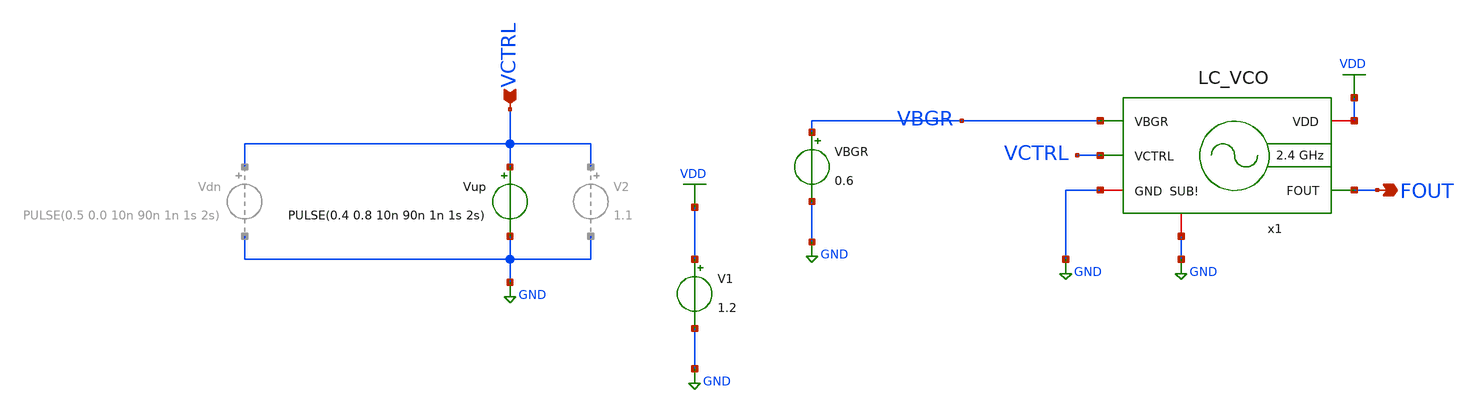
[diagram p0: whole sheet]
** sch_path: xschem/lc-vco/LC_VCO_tb.sch
**.subckt LC_VCO_tb FOUT VCTRL
*.opin FOUT
*.ipin VCTRL
VBGR VBGR GND 0.6
x1 VDD VCTRL GND FOUT VBGR GND LC_VCO
V1 VDD GND 1.2
Vup VCTRL GND PULSE(0.4 0.8 10n 90n 1n 1s 2s)
**** begin user architecture code



.param temp = 27
.options method=gear rshunt=1.0e12

.control

* Save required signals
save v(VCTRL) v(FOUT) v(x1.Vx) v(x1.OUTp)

* Long transient simulation
tran 10p 500n 100n

* Save raw waveform
write tb_LC_VCO_tran.raw

* Plot transient waveform
let vout = v(FOUT)
plot v(VCTRL) v(x1.Vx) v(FOUT) v(x1.OUTp)

* Plot steady-state waveform
plot v(VCTRL) v(x1.Vx) v(FOUT) v(x1.OUTp) xlimit 400n 405n

* FFT analysis
setplot tran1
linearize vout
set specwindow=blackman
fft vout

* Plot FFT spectrum
let power_out_db = db(vout)
plot power_out_db xlimit 2.34G 2.54G ylimit -200 0

* Find the maximum magnitude value between 2G and 3G
meas sp max_power_out_db max power_out_db FROM=2G TO=3G

* Save FFT spectrum as raw file
write LC_VCO_fft.raw frequency power_out_db
shell python3 ../xschem/lc-vco/raw_spectrum_as_tran.py LC_VCO_fft.raw

* Save FFT data
wrdata fft_output_standalone.txt frequency power_out_db

* Save waveform for external processing
wrdata vco_waveform_standalone.txt power_out_db

.endc






.param temp=27
.control
save all
op
write LC_VCO_tb.raw
.endc




.include 4nH_INDUCTOR.spice


.lib cornerMOSlv.lib mos_tt
.lib cornerMOShv.lib mos_tt
.lib cornerRES.lib res_typ
.lib cornerCAP.lib cap_typ

**** end user architecture code
**.ends

* expanding   symbol:  xschem/lc-vco/LC_VCO.sym # of pins=6
** sym_path: xschem/lc-vco/LC_VCO.sym
** sch_path: xschem/lc-vco/LC_VCO.sch
.subckt LC_VCO VDD VCTRL GND FOUT VBGR SUB!
*.opin FOUT
*.ipin VCTRL
*.ipin VBGR
*.iopin VDD
*.iopin GND
*.iopin SUB!
x1 OUTn OUTp 4nH_INDUCTOR
**** begin user architecture code


.subckt 4nH_INDUCTOR 1 2
* LVS black-box stub only
* Full model is available in 4nH_INDUCTOR.spice
.ends


**** end user architecture code
XM5 Vx Vgs GND SUB! sg13_lv_nmos w=384u l=1u ng=48 m=1 mm_ok=1
XM4 OUTp OUTn VDD NW sg13_lv_pmos w=36u l=0.13u ng=5 m=1 mm_ok=1
XM3 OUTn OUTp VDD NW sg13_lv_pmos w=36u l=0.13u ng=5 m=1 mm_ok=1
XM2 OUTp OUTn Vx SUB! sg13_lv_nmos w=21.99u l=0.13u ng=3 m=1 mm_ok=1
XM1 OUTn OUTp Vx SUB! sg13_lv_nmos w=21.99u l=0.13u ng=3 m=1 mm_ok=1
XM6 Vgs Vgs GND SUB! sg13_lv_nmos w=64u l=1u ng=8 m=1 mm_ok=1
XC1 OUTn OUTp SUB! cap_rfcmim w=21.9e-6 l=21.9e-6 wfeed=10.0e-6 m=1 mm_ok=1
XC3 OUTp VCTRL OUTn sub! sg13_hv_svaricap w=9.74u l=0.8u Nx=7 mm_ok=1
XC2 OUTp VCTRL OUTn sub! sg13_hv_svaricap w=9.74u l=0.8u Nx=7 mm_ok=1
XM7 Vgs VBGR VDD NWa sg13_lv_pmos w=38u l=1u ng=5 m=1 mm_ok=1
XM8 FOUT OUTp VDD NW sg13_lv_pmos w=15u l=0.13u ng=10 m=1 mm_ok=1
XM9 FOUT OUTp GND SUB! sg13_lv_nmos w=1.5u l=0.13u ng=1 m=1 mm_ok=1
XM10 net1 OUTn VDD NW sg13_lv_pmos w=15u l=0.13u ng=10 m=1 mm_ok=1
XM11 net1 OUTn GND SUB! sg13_lv_nmos w=1.5u l=0.13u ng=1 m=1 mm_ok=1
XR1 VDD NW ntap1 R=7.357 w=10.22e-6 l=5.87e-6 rw=0.3e-6
XR2 VDD NW ntap1 R=7.357 w=10.22e-6 l=5.87e-6 rw=0.3e-6
XR3 GND SUB! ptap1 R=2.388 w=33.9e-6 l=14.41e-6 rw=0.3e-6
XR4 GND SUB! ptap1 R=8.306 w=10.09e-6 l=4.23e-6 rw=0.3e-6
XR5 GND SUB! ptap1 R=8.306 w=10.09e-6 l=4.23e-6 rw=0.3e-6
XR6 VDD NW ntap1 R=9.234 w=8.42e-6 l=4.52e-6 rw=0.3e-6
XR7 VDD NW ntap1 R=9.234 w=8.42e-6 l=4.52e-6 rw=0.3e-6
XR8 GND SUB! ptap1 R=16.59 w=3.21e-6 l=4.26e-6 rw=0.3e-6
XR9 GND SUB! ptap1 R=16.59 w=3.21e-6 l=4.26e-6 rw=0.3e-6
XR10 GND SUB! ptap1 R=4.768 w=10.76e-6 l=13.74e-6 rw=0.3e-6
XR11 GND SUB! ptap1 R=1.636 w=12.36e-6 l=57.9e-6 rw=0.3e-6
XR12 VDD NWa ntap1 R=5.63 w=10.62e-6 l=10.22e-6 rw=0.3e-6
.ends

.GLOBAL GND
.GLOBAL VDD
.end
